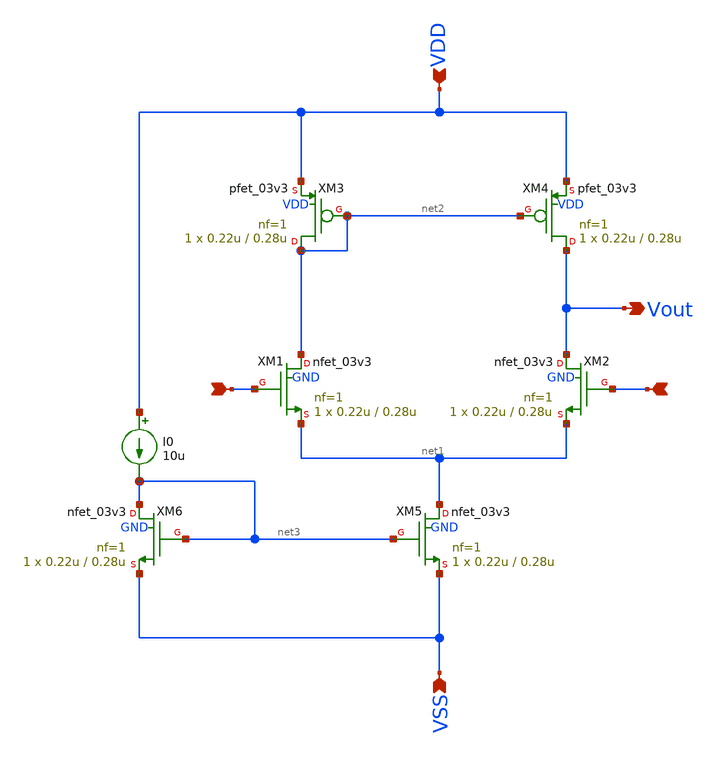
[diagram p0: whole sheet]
** sch_path: xschem/ota_miller/ota_n_in.sch
**.subckt ota_n_in Vout VSS VDD + -
*.opin Vout
*.ipin VSS
*.ipin VDD
*.ipin +
*.ipin -
I0 VDD net3 10u
XM1 net2 + net1 GND nfet_03v3 L=0.28u W=0.22u nf=1 ad='int((nf+1)/2) * W/nf * 0.18u' as='int((nf+2)/2) * W/nf * 0.18u'
+ pd='2*int((nf+1)/2) * (W/nf + 0.18u)' ps='2*int((nf+2)/2) * (W/nf + 0.18u)' nrd='0.18u / W' nrs='0.18u / W'
+ sa=0 sb=0 sd=0 m=1 par=1
XM2 Vout - net1 GND nfet_03v3 L=0.28u W=0.22u nf=1 ad='int((nf+1)/2) * W/nf * 0.18u' as='int((nf+2)/2) * W/nf * 0.18u'
+ pd='2*int((nf+1)/2) * (W/nf + 0.18u)' ps='2*int((nf+2)/2) * (W/nf + 0.18u)' nrd='0.18u / W' nrs='0.18u / W'
+ sa=0 sb=0 sd=0 m=1 par=1
XM3 net2 net2 VDD VDD pfet_03v3 L=0.28u W=0.22u nf=1 ad='int((nf+1)/2) * W/nf * 0.18u' as='int((nf+2)/2) * W/nf * 0.18u'
+ pd='2*int((nf+1)/2) * (W/nf + 0.18u)' ps='2*int((nf+2)/2) * (W/nf + 0.18u)' nrd='0.18u / W' nrs='0.18u / W'
+ sa=0 sb=0 sd=0 m=1 par=1
XM4 Vout net2 VDD VDD pfet_03v3 L=0.28u W=0.22u nf=1 ad='int((nf+1)/2) * W/nf * 0.18u' as='int((nf+2)/2) * W/nf * 0.18u'
+ pd='2*int((nf+1)/2) * (W/nf + 0.18u)' ps='2*int((nf+2)/2) * (W/nf + 0.18u)' nrd='0.18u / W' nrs='0.18u / W'
+ sa=0 sb=0 sd=0 m=1 par=1
XM5 net1 net3 VSS GND nfet_03v3 L=0.28u W=0.22u nf=1 ad='int((nf+1)/2) * W/nf * 0.18u' as='int((nf+2)/2) * W/nf * 0.18u'
+ pd='2*int((nf+1)/2) * (W/nf + 0.18u)' ps='2*int((nf+2)/2) * (W/nf + 0.18u)' nrd='0.18u / W' nrs='0.18u / W'
+ sa=0 sb=0 sd=0 m=1 par=1
XM6 net3 net3 VSS GND nfet_03v3 L=0.28u W=0.22u nf=1 ad='int((nf+1)/2) * W/nf * 0.18u' as='int((nf+2)/2) * W/nf * 0.18u'
+ pd='2*int((nf+1)/2) * (W/nf + 0.18u)' ps='2*int((nf+2)/2) * (W/nf + 0.18u)' nrd='0.18u / W' nrs='0.18u / W'
+ sa=0 sb=0 sd=0 m=1 par=1
**.ends
.end
